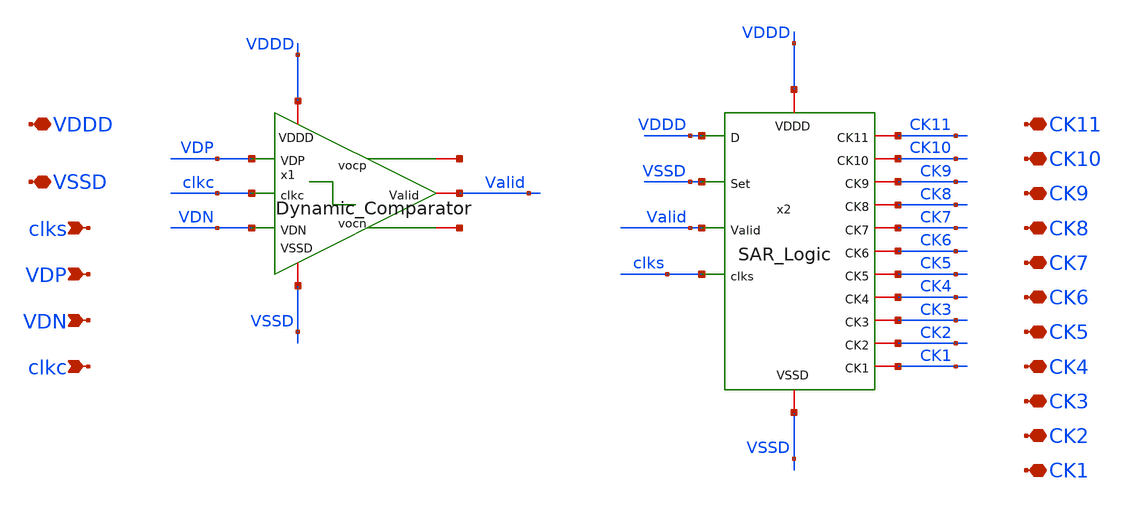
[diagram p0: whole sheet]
** sch_path: SAR_ADC/integration/DynComp_SARLogic.sch
**.subckt DynComp_SARLogic VDDD VSSD clks VDP VDN CK11 CK10 CK9 CK8 CK7 CK6 CK5 CK4 CK3 CK2 CK1 clkc
*.iopin VDDD
*.iopin VSSD
*.ipin clks
*.ipin VDP
*.ipin VDN
*.iopin CK11
*.iopin CK10
*.iopin CK9
*.iopin CK8
*.iopin CK7
*.iopin CK6
*.iopin CK5
*.iopin CK4
*.iopin CK3
*.iopin CK2
*.iopin CK1
*.ipin clkc
x1 net1 net2 VDDD VSSD VDP VDN Valid clkc Dynamic_Comparator
x2 CK11 VDDD CK1 CK6 VSSD CK10 CK5 CK9 CK4 clks CK8 CK3 Valid CK2 CK7 VSSD VDDD SAR_Logic
**.ends
.end
